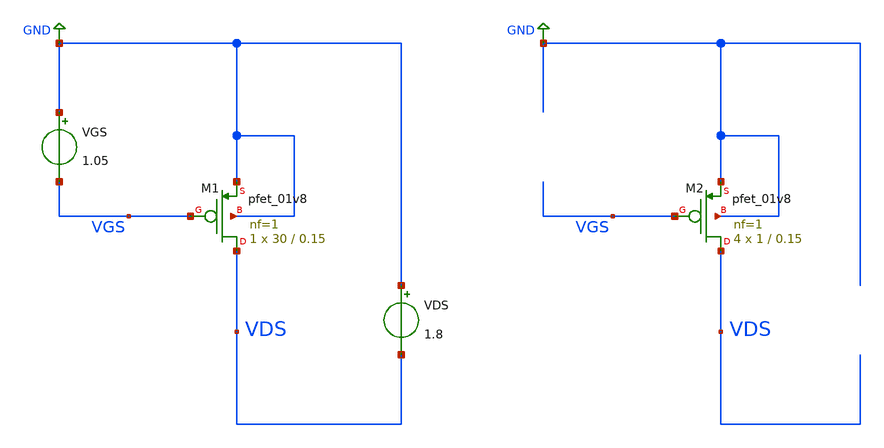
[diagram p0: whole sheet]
** sch_path: projects/opamp/xschem_ngspice/vds_vgs_sweep_pfet_2.sch
**.subckt vds_vgs_sweep_pfet_2
VGS GND VGS 1.05
VDS GND VDS 1.8
XM1 VDS VGS GND GND sky130_fd_pr__pfet_01v8 L=0.15 W=30 nf=1 ad='int((nf+1)/2) * W/nf * 0.29' as='int((nf+2)/2) * W/nf * 0.29'
+ pd='2*int((nf+1)/2) * (W/nf + 0.29)' ps='2*int((nf+2)/2) * (W/nf + 0.29)' nrd='0.29 / W' nrs='0.29 / W'
+ sa=0 sb=0 sd=0 mult=1 m=1
XM2 VDS VGS GND GND sky130_fd_pr__pfet_01v8 L=0.15 W=1 nf=1 ad='int((nf+1)/2) * W/nf * 0.29' as='int((nf+2)/2) * W/nf * 0.29'
+ pd='2*int((nf+1)/2) * (W/nf + 0.29)' ps='2*int((nf+2)/2) * (W/nf + 0.29)' nrd='0.29 / W' nrs='0.29 / W'
+ sa=0 sb=0 sd=0 mult=4 m=4
**** begin user architecture code
.lib $::SKYWATER_MODELS/sky130.lib.spice tt



.option method=gear
.option wnflag=1
.option savecurrents
*.temp = 120

.save @m.xm1.msky130_fd_pr__pfet_01v8[gm] @m.xm1.msky130_fd_pr__pfet_01v8[vth] @m.xm2.msky130_fd_pr__pfet_01v8[gm] @m.xm2.msky130_fd_pr__pfet_01v8[vth] @m.xm3.msky130_fd_pr__pfet_01v8[gm] @m.xm4.msky130_fd_pr__pfet_01v8[gm] @m.xm5.msky130_fd_pr__pfet_01v8[gm] @m.xm6.msky130_fd_pr__pfet_01v8[gm] @m.xm7.msky130_fd_pr__pfet_01v8[gm] @m.xm8.msky130_fd_pr__pfet_01v8[gm] @m.xm9.msky130_fd_pr__pfet_01v8[gm] @m.xm10.msky130_fd_pr__pfet_01v8[gm]


.control
  save all
  * dc VGS 0 1.8 0.1 VDS 0 1.8 0.1
  * dc VDS 0 1.0 0.001 VGS 0.6 1.3 0.01
  dc VDS 0.1 0.9 0.001 VGS 0.3 1.6 0.01
  remzerovec
  write vds_vgs_sweep_pfet_2.raw
  set appendwrite
  let rout = deriv(vds)/deriv(@m.xm10.msky130_fd_pr__pfet_01v8[id])
  save rout
  show
.endc



**** end user architecture code
**.ends
.GLOBAL GND
.end
